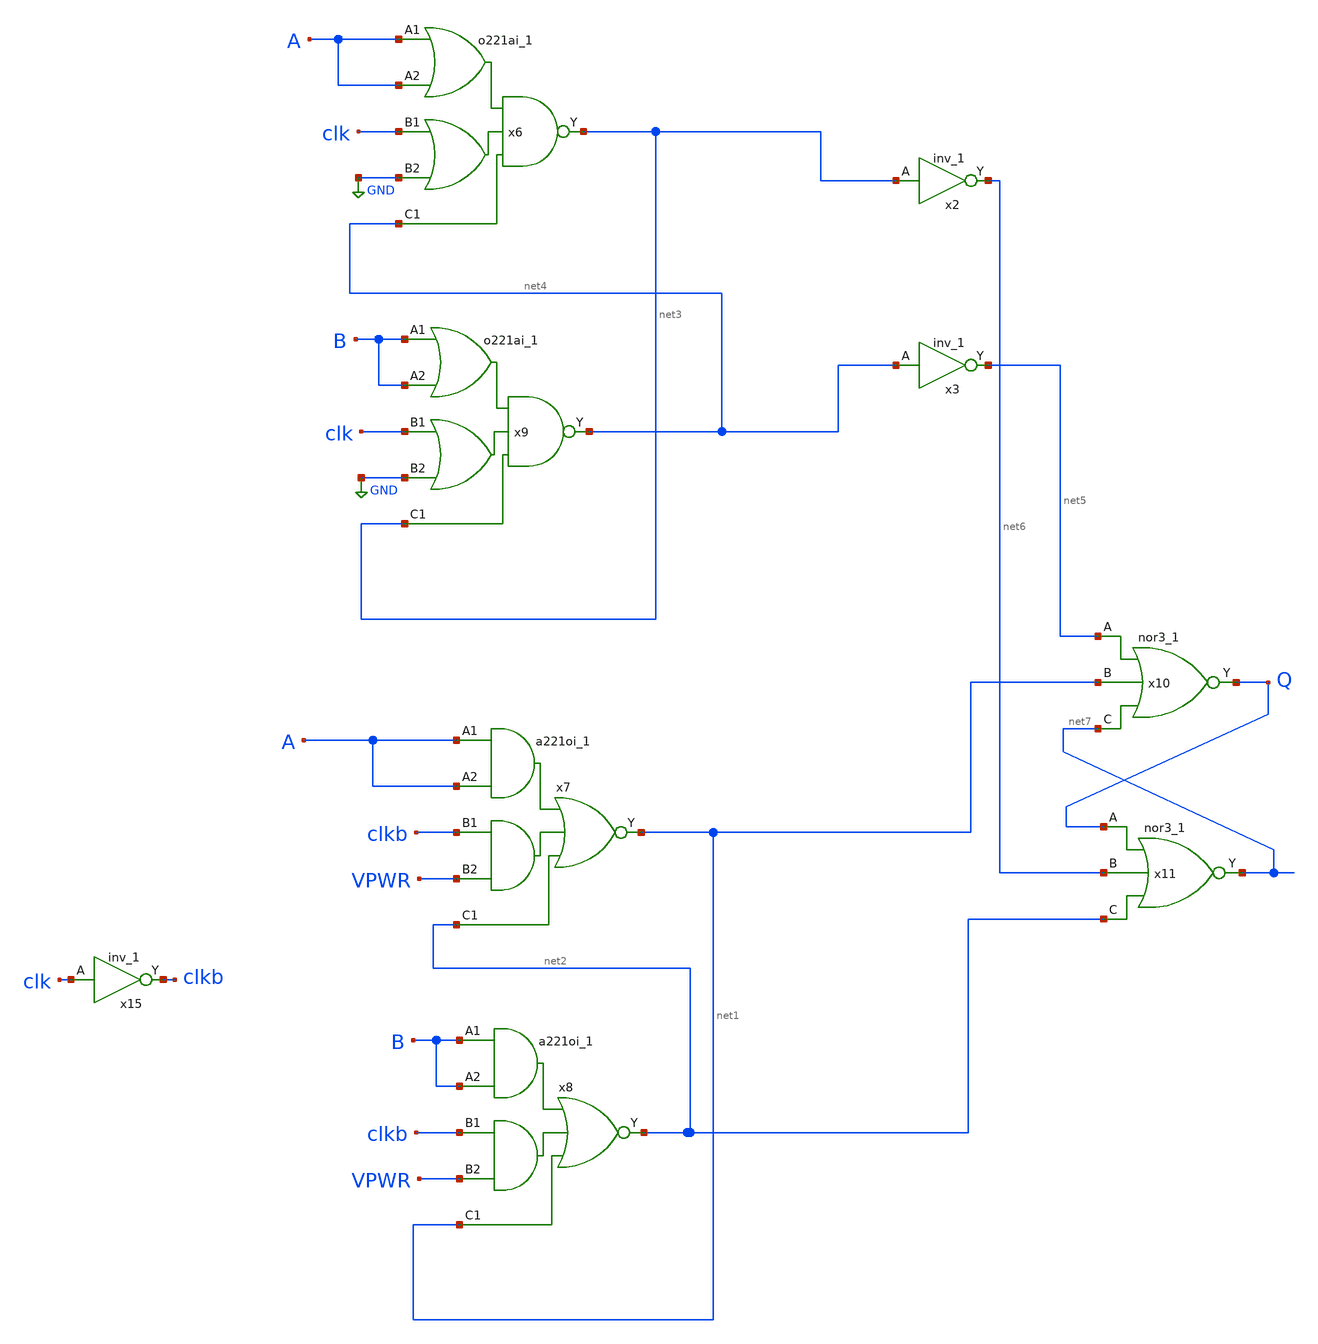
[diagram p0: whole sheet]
** sch_path: cmp/Schematics/cmpoai_all_.sch
**.subckt cmpoai_all_
x15 clk VGND VNB VPB VPWR clkb sky130_fd_sc_hd__inv_1
x7 A A clkb VPWR net2 VGND VNB VPB VPWR net1 sky130_fd_sc_hd__a221oi_1
x8 B B clkb VPWR net1 VGND VNB VPB VPWR net2 sky130_fd_sc_hd__a221oi_1
x2 net3 VGND VNB VPB VPWR net6 sky130_fd_sc_hd__inv_1
x3 net4 VGND VNB VPB VPWR net5 sky130_fd_sc_hd__inv_1
x6 A A clk GND net4 VGND VNB VPB VPWR net3 sky130_fd_sc_hd__o221ai_1
x9 B B clk GND net3 VGND VNB VPB VPWR net4 sky130_fd_sc_hd__o221ai_1
x10 net5 net1 net7 VGND VNB VPB VPWR Q sky130_fd_sc_hd__nor3_1
x11 Q net6 net2 VGND VNB VPB VPWR net7 sky130_fd_sc_hd__nor3_1
**.ends
.GLOBAL GND
.end
